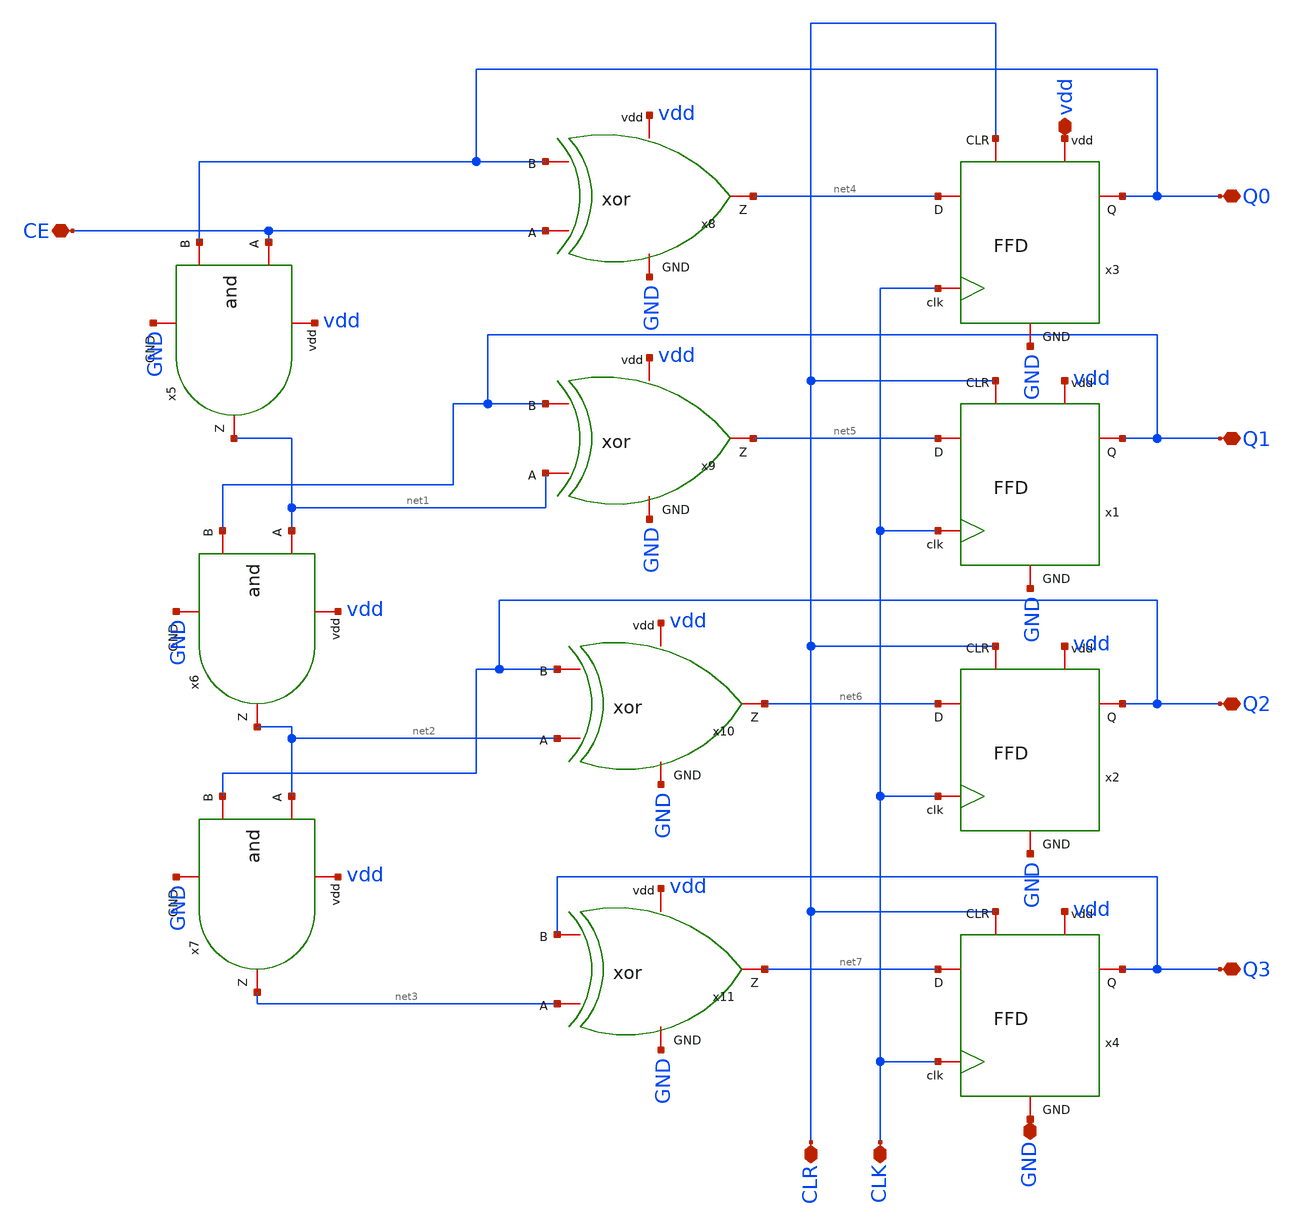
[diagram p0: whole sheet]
** sch_path: simbolos y esquematicos/cont4.sch
**.subckt cont4 CE Q0 Q1 Q2 Q3 CLK CLR GND vdd
*.iopin CE
*.iopin Q0
*.iopin Q1
*.iopin Q2
*.iopin Q3
*.iopin CLK
*.iopin CLR
*.iopin GND
*.iopin vdd
x1 vdd GND CLR Q1 net5 CLK FFD
x2 vdd GND CLR Q2 net6 CLK FFD
x3 vdd GND CLR Q0 net4 CLK FFD
x4 vdd GND CLR Q3 net7 CLK FFD
x5 vdd CE net1 Q0 GND and
x6 vdd net1 net2 Q1 GND and
x7 vdd net2 net3 Q2 GND and
x8 vdd CE Q0 net4 GND xor
x9 vdd net1 Q1 net5 GND xor
x10 vdd net2 Q2 net6 GND xor
x11 vdd net3 Q3 net7 GND xor
**.ends
.end
